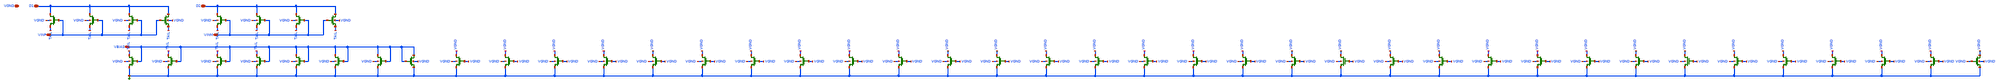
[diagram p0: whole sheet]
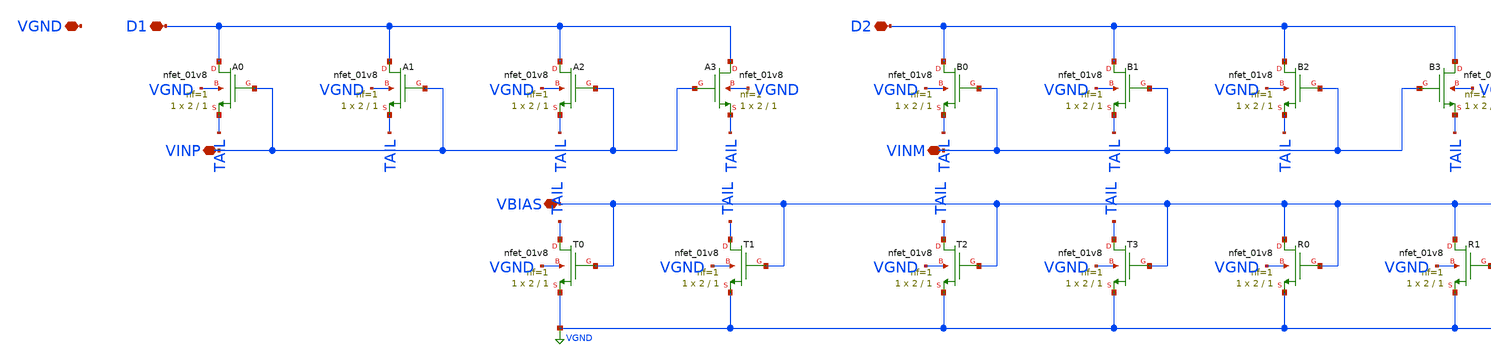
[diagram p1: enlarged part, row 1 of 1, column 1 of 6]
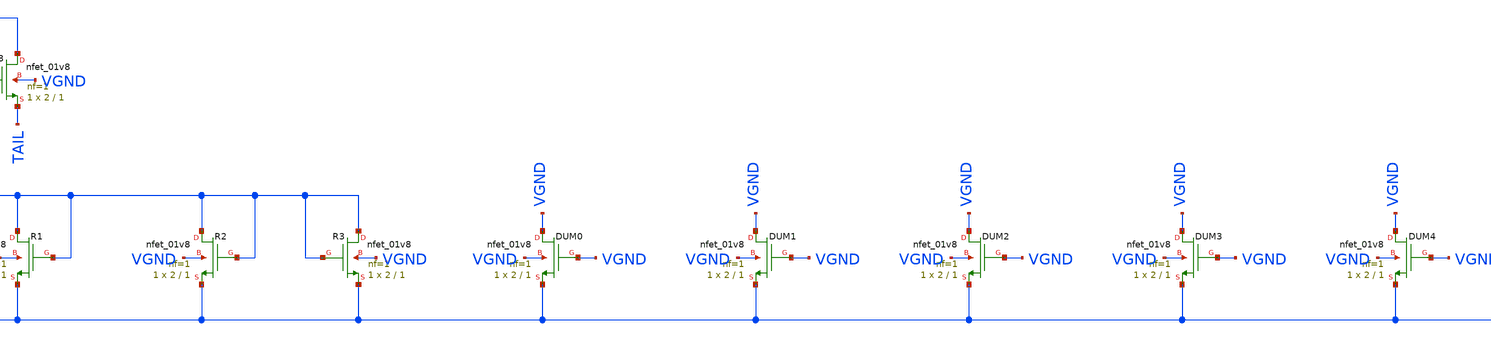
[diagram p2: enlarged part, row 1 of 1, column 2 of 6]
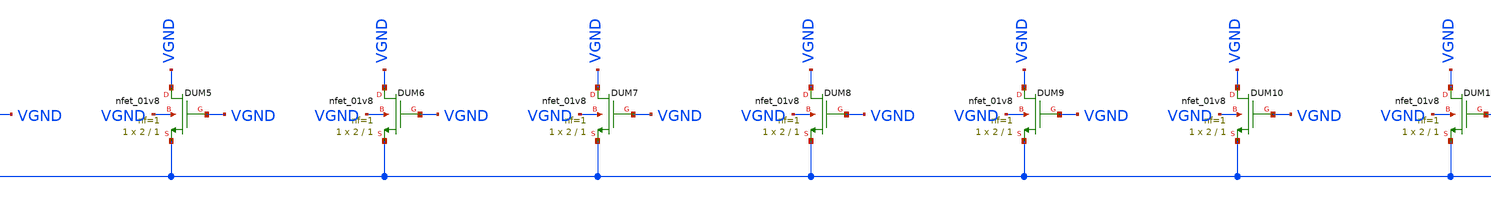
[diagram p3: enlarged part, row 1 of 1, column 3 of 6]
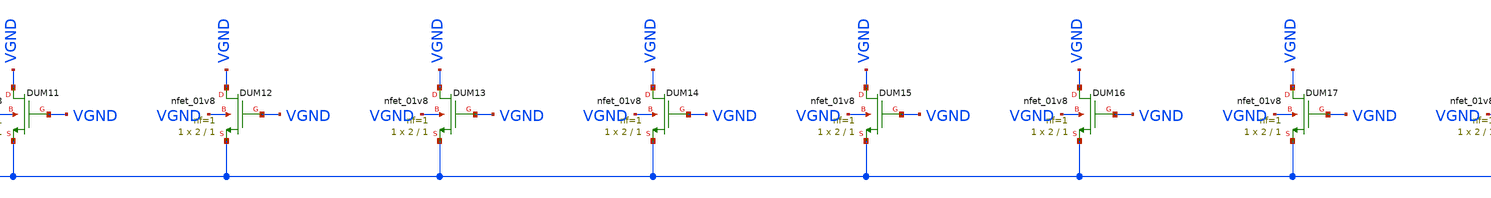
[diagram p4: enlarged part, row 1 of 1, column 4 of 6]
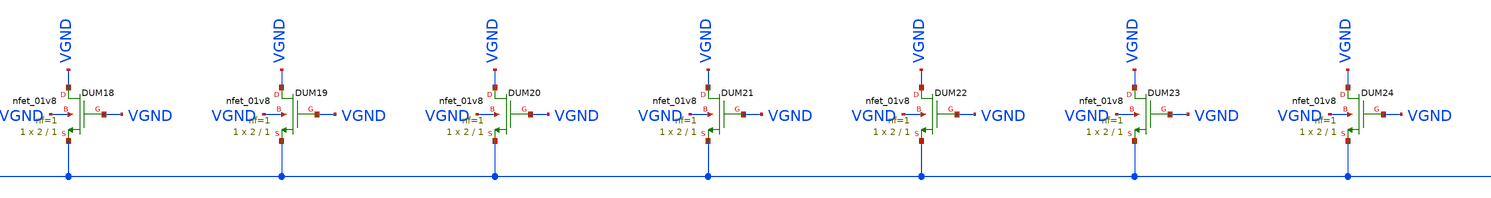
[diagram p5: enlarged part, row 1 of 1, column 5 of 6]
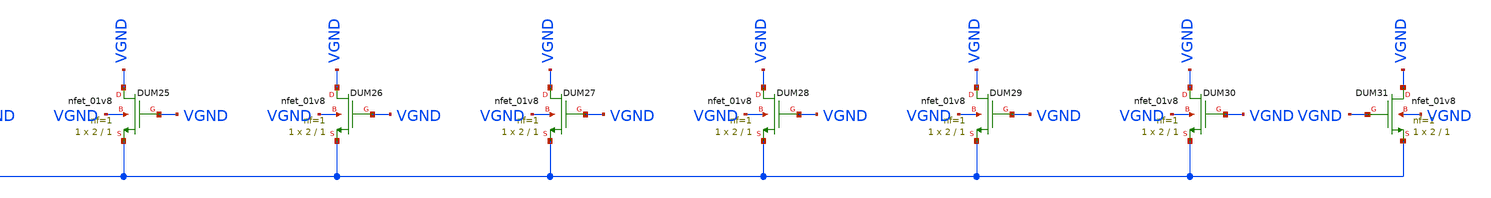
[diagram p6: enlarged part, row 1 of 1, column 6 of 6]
** sch_path: cells/ELAD1_PAIR_GROUPED/schematic/ELAD1_PAIR_GROUPED.sch
**.subckt ELAD1_PAIR_GROUPED VINP VINM D1 D2 VBIAS VGND
*.iopin VINP
*.iopin VINM
*.iopin D1
*.iopin D2
*.iopin VBIAS
*.iopin VGND
XA0 D1 VINP TAIL VGND sky130_fd_pr__nfet_01v8 L=1 W=2 nf=1 ad='int((1 + 1)/2) * 2 / 1 * 0.29' as='int((1 + 2)/2) * 2 / 1 * 0.29'
+ pd='2*int((1 + 1)/2) * (2 / 1 + 0.29)' ps='2*int((1 + 2)/2) * (2 / 1 + 0.29)' nrd='0.29 / 2 ' nrs='0.29 / 2 '
+ sa=0 sb=0 sd=0 mult=1 m=1
XA1 D1 VINP TAIL VGND sky130_fd_pr__nfet_01v8 L=1 W=2 nf=1 ad='int((1 + 1)/2) * 2 / 1 * 0.29' as='int((1 + 2)/2) * 2 / 1 * 0.29'
+ pd='2*int((1 + 1)/2) * (2 / 1 + 0.29)' ps='2*int((1 + 2)/2) * (2 / 1 + 0.29)' nrd='0.29 / 2 ' nrs='0.29 / 2 '
+ sa=0 sb=0 sd=0 mult=1 m=1
XA2 D1 VINP TAIL VGND sky130_fd_pr__nfet_01v8 L=1 W=2 nf=1 ad='int((1 + 1)/2) * 2 / 1 * 0.29' as='int((1 + 2)/2) * 2 / 1 * 0.29'
+ pd='2*int((1 + 1)/2) * (2 / 1 + 0.29)' ps='2*int((1 + 2)/2) * (2 / 1 + 0.29)' nrd='0.29 / 2 ' nrs='0.29 / 2 '
+ sa=0 sb=0 sd=0 mult=1 m=1
XA3 D1 VINP TAIL VGND sky130_fd_pr__nfet_01v8 L=1 W=2 nf=1 ad='int((1 + 1)/2) * 2 / 1 * 0.29' as='int((1 + 2)/2) * 2 / 1 * 0.29'
+ pd='2*int((1 + 1)/2) * (2 / 1 + 0.29)' ps='2*int((1 + 2)/2) * (2 / 1 + 0.29)' nrd='0.29 / 2 ' nrs='0.29 / 2 '
+ sa=0 sb=0 sd=0 mult=1 m=1
XB0 D2 VINM TAIL VGND sky130_fd_pr__nfet_01v8 L=1 W=2 nf=1 ad='int((1 + 1)/2) * 2 / 1 * 0.29' as='int((1 + 2)/2) * 2 / 1 * 0.29'
+ pd='2*int((1 + 1)/2) * (2 / 1 + 0.29)' ps='2*int((1 + 2)/2) * (2 / 1 + 0.29)' nrd='0.29 / 2 ' nrs='0.29 / 2 '
+ sa=0 sb=0 sd=0 mult=1 m=1
XB1 D2 VINM TAIL VGND sky130_fd_pr__nfet_01v8 L=1 W=2 nf=1 ad='int((1 + 1)/2) * 2 / 1 * 0.29' as='int((1 + 2)/2) * 2 / 1 * 0.29'
+ pd='2*int((1 + 1)/2) * (2 / 1 + 0.29)' ps='2*int((1 + 2)/2) * (2 / 1 + 0.29)' nrd='0.29 / 2 ' nrs='0.29 / 2 '
+ sa=0 sb=0 sd=0 mult=1 m=1
XB2 D2 VINM TAIL VGND sky130_fd_pr__nfet_01v8 L=1 W=2 nf=1 ad='int((1 + 1)/2) * 2 / 1 * 0.29' as='int((1 + 2)/2) * 2 / 1 * 0.29'
+ pd='2*int((1 + 1)/2) * (2 / 1 + 0.29)' ps='2*int((1 + 2)/2) * (2 / 1 + 0.29)' nrd='0.29 / 2 ' nrs='0.29 / 2 '
+ sa=0 sb=0 sd=0 mult=1 m=1
XB3 D2 VINM TAIL VGND sky130_fd_pr__nfet_01v8 L=1 W=2 nf=1 ad='int((1 + 1)/2) * 2 / 1 * 0.29' as='int((1 + 2)/2) * 2 / 1 * 0.29'
+ pd='2*int((1 + 1)/2) * (2 / 1 + 0.29)' ps='2*int((1 + 2)/2) * (2 / 1 + 0.29)' nrd='0.29 / 2 ' nrs='0.29 / 2 '
+ sa=0 sb=0 sd=0 mult=1 m=1
XT0 TAIL VBIAS VGND VGND sky130_fd_pr__nfet_01v8 L=1 W=2 nf=1 ad='int((1 + 1)/2) * 2 / 1 * 0.29' as='int((1 + 2)/2) * 2 / 1 * 0.29'
+ pd='2*int((1 + 1)/2) * (2 / 1 + 0.29)' ps='2*int((1 + 2)/2) * (2 / 1 + 0.29)' nrd='0.29 / 2 ' nrs='0.29 / 2 '
+ sa=0 sb=0 sd=0 mult=1 m=1
XT1 TAIL VBIAS VGND VGND sky130_fd_pr__nfet_01v8 L=1 W=2 nf=1 ad='int((1 + 1)/2) * 2 / 1 * 0.29' as='int((1 + 2)/2) * 2 / 1 * 0.29'
+ pd='2*int((1 + 1)/2) * (2 / 1 + 0.29)' ps='2*int((1 + 2)/2) * (2 / 1 + 0.29)' nrd='0.29 / 2 ' nrs='0.29 / 2 '
+ sa=0 sb=0 sd=0 mult=1 m=1
XT2 TAIL VBIAS VGND VGND sky130_fd_pr__nfet_01v8 L=1 W=2 nf=1 ad='int((1 + 1)/2) * 2 / 1 * 0.29' as='int((1 + 2)/2) * 2 / 1 * 0.29'
+ pd='2*int((1 + 1)/2) * (2 / 1 + 0.29)' ps='2*int((1 + 2)/2) * (2 / 1 + 0.29)' nrd='0.29 / 2 ' nrs='0.29 / 2 '
+ sa=0 sb=0 sd=0 mult=1 m=1
XT3 TAIL VBIAS VGND VGND sky130_fd_pr__nfet_01v8 L=1 W=2 nf=1 ad='int((1 + 1)/2) * 2 / 1 * 0.29' as='int((1 + 2)/2) * 2 / 1 * 0.29'
+ pd='2*int((1 + 1)/2) * (2 / 1 + 0.29)' ps='2*int((1 + 2)/2) * (2 / 1 + 0.29)' nrd='0.29 / 2 ' nrs='0.29 / 2 '
+ sa=0 sb=0 sd=0 mult=1 m=1
XR0 VBIAS VBIAS VGND VGND sky130_fd_pr__nfet_01v8 L=1 W=2 nf=1 ad='int((1 + 1)/2) * 2 / 1 * 0.29' as='int((1 + 2)/2) * 2 / 1 * 0.29'
+ pd='2*int((1 + 1)/2) * (2 / 1 + 0.29)' ps='2*int((1 + 2)/2) * (2 / 1 + 0.29)' nrd='0.29 / 2 ' nrs='0.29 / 2 '
+ sa=0 sb=0 sd=0 mult=1 m=1
XR1 VBIAS VBIAS VGND VGND sky130_fd_pr__nfet_01v8 L=1 W=2 nf=1 ad='int((1 + 1)/2) * 2 / 1 * 0.29' as='int((1 + 2)/2) * 2 / 1 * 0.29'
+ pd='2*int((1 + 1)/2) * (2 / 1 + 0.29)' ps='2*int((1 + 2)/2) * (2 / 1 + 0.29)' nrd='0.29 / 2 ' nrs='0.29 / 2 '
+ sa=0 sb=0 sd=0 mult=1 m=1
XR2 VBIAS VBIAS VGND VGND sky130_fd_pr__nfet_01v8 L=1 W=2 nf=1 ad='int((1 + 1)/2) * 2 / 1 * 0.29' as='int((1 + 2)/2) * 2 / 1 * 0.29'
+ pd='2*int((1 + 1)/2) * (2 / 1 + 0.29)' ps='2*int((1 + 2)/2) * (2 / 1 + 0.29)' nrd='0.29 / 2 ' nrs='0.29 / 2 '
+ sa=0 sb=0 sd=0 mult=1 m=1
XR3 VBIAS VBIAS VGND VGND sky130_fd_pr__nfet_01v8 L=1 W=2 nf=1 ad='int((1 + 1)/2) * 2 / 1 * 0.29' as='int((1 + 2)/2) * 2 / 1 * 0.29'
+ pd='2*int((1 + 1)/2) * (2 / 1 + 0.29)' ps='2*int((1 + 2)/2) * (2 / 1 + 0.29)' nrd='0.29 / 2 ' nrs='0.29 / 2 '
+ sa=0 sb=0 sd=0 mult=1 m=1
XDUM0 VGND VGND VGND VGND sky130_fd_pr__nfet_01v8 L=1 W=2 nf=1 ad='int((1 + 1)/2) * 2 / 1 * 0.29' as='int((1 + 2)/2) * 2 / 1 * 0.29'
+ pd='2*int((1 + 1)/2) * (2 / 1 + 0.29)' ps='2*int((1 + 2)/2) * (2 / 1 + 0.29)' nrd='0.29 / 2 ' nrs='0.29 / 2 '
+ sa=0 sb=0 sd=0 mult=1 m=1
XDUM1 VGND VGND VGND VGND sky130_fd_pr__nfet_01v8 L=1 W=2 nf=1 ad='int((1 + 1)/2) * 2 / 1 * 0.29' as='int((1 + 2)/2) * 2 / 1 * 0.29'
+ pd='2*int((1 + 1)/2) * (2 / 1 + 0.29)' ps='2*int((1 + 2)/2) * (2 / 1 + 0.29)' nrd='0.29 / 2 ' nrs='0.29 / 2 '
+ sa=0 sb=0 sd=0 mult=1 m=1
XDUM2 VGND VGND VGND VGND sky130_fd_pr__nfet_01v8 L=1 W=2 nf=1 ad='int((1 + 1)/2) * 2 / 1 * 0.29' as='int((1 + 2)/2) * 2 / 1 * 0.29'
+ pd='2*int((1 + 1)/2) * (2 / 1 + 0.29)' ps='2*int((1 + 2)/2) * (2 / 1 + 0.29)' nrd='0.29 / 2 ' nrs='0.29 / 2 '
+ sa=0 sb=0 sd=0 mult=1 m=1
XDUM3 VGND VGND VGND VGND sky130_fd_pr__nfet_01v8 L=1 W=2 nf=1 ad='int((1 + 1)/2) * 2 / 1 * 0.29' as='int((1 + 2)/2) * 2 / 1 * 0.29'
+ pd='2*int((1 + 1)/2) * (2 / 1 + 0.29)' ps='2*int((1 + 2)/2) * (2 / 1 + 0.29)' nrd='0.29 / 2 ' nrs='0.29 / 2 '
+ sa=0 sb=0 sd=0 mult=1 m=1
XDUM4 VGND VGND VGND VGND sky130_fd_pr__nfet_01v8 L=1 W=2 nf=1 ad='int((1 + 1)/2) * 2 / 1 * 0.29' as='int((1 + 2)/2) * 2 / 1 * 0.29'
+ pd='2*int((1 + 1)/2) * (2 / 1 + 0.29)' ps='2*int((1 + 2)/2) * (2 / 1 + 0.29)' nrd='0.29 / 2 ' nrs='0.29 / 2 '
+ sa=0 sb=0 sd=0 mult=1 m=1
XDUM5 VGND VGND VGND VGND sky130_fd_pr__nfet_01v8 L=1 W=2 nf=1 ad='int((1 + 1)/2) * 2 / 1 * 0.29' as='int((1 + 2)/2) * 2 / 1 * 0.29'
+ pd='2*int((1 + 1)/2) * (2 / 1 + 0.29)' ps='2*int((1 + 2)/2) * (2 / 1 + 0.29)' nrd='0.29 / 2 ' nrs='0.29 / 2 '
+ sa=0 sb=0 sd=0 mult=1 m=1
XDUM6 VGND VGND VGND VGND sky130_fd_pr__nfet_01v8 L=1 W=2 nf=1 ad='int((1 + 1)/2) * 2 / 1 * 0.29' as='int((1 + 2)/2) * 2 / 1 * 0.29'
+ pd='2*int((1 + 1)/2) * (2 / 1 + 0.29)' ps='2*int((1 + 2)/2) * (2 / 1 + 0.29)' nrd='0.29 / 2 ' nrs='0.29 / 2 '
+ sa=0 sb=0 sd=0 mult=1 m=1
XDUM7 VGND VGND VGND VGND sky130_fd_pr__nfet_01v8 L=1 W=2 nf=1 ad='int((1 + 1)/2) * 2 / 1 * 0.29' as='int((1 + 2)/2) * 2 / 1 * 0.29'
+ pd='2*int((1 + 1)/2) * (2 / 1 + 0.29)' ps='2*int((1 + 2)/2) * (2 / 1 + 0.29)' nrd='0.29 / 2 ' nrs='0.29 / 2 '
+ sa=0 sb=0 sd=0 mult=1 m=1
XDUM8 VGND VGND VGND VGND sky130_fd_pr__nfet_01v8 L=1 W=2 nf=1 ad='int((1 + 1)/2) * 2 / 1 * 0.29' as='int((1 + 2)/2) * 2 / 1 * 0.29'
+ pd='2*int((1 + 1)/2) * (2 / 1 + 0.29)' ps='2*int((1 + 2)/2) * (2 / 1 + 0.29)' nrd='0.29 / 2 ' nrs='0.29 / 2 '
+ sa=0 sb=0 sd=0 mult=1 m=1
XDUM9 VGND VGND VGND VGND sky130_fd_pr__nfet_01v8 L=1 W=2 nf=1 ad='int((1 + 1)/2) * 2 / 1 * 0.29' as='int((1 + 2)/2) * 2 / 1 * 0.29'
+ pd='2*int((1 + 1)/2) * (2 / 1 + 0.29)' ps='2*int((1 + 2)/2) * (2 / 1 + 0.29)' nrd='0.29 / 2 ' nrs='0.29 / 2 '
+ sa=0 sb=0 sd=0 mult=1 m=1
XDUM10 VGND VGND VGND VGND sky130_fd_pr__nfet_01v8 L=1 W=2 nf=1 ad='int((1 + 1)/2) * 2 / 1 * 0.29' as='int((1 + 2)/2) * 2 / 1 * 0.29'
+ pd='2*int((1 + 1)/2) * (2 / 1 + 0.29)' ps='2*int((1 + 2)/2) * (2 / 1 + 0.29)' nrd='0.29 / 2 ' nrs='0.29 / 2 '
+ sa=0 sb=0 sd=0 mult=1 m=1
XDUM11 VGND VGND VGND VGND sky130_fd_pr__nfet_01v8 L=1 W=2 nf=1 ad='int((1 + 1)/2) * 2 / 1 * 0.29' as='int((1 + 2)/2) * 2 / 1 * 0.29'
+ pd='2*int((1 + 1)/2) * (2 / 1 + 0.29)' ps='2*int((1 + 2)/2) * (2 / 1 + 0.29)' nrd='0.29 / 2 ' nrs='0.29 / 2 '
+ sa=0 sb=0 sd=0 mult=1 m=1
XDUM12 VGND VGND VGND VGND sky130_fd_pr__nfet_01v8 L=1 W=2 nf=1 ad='int((1 + 1)/2) * 2 / 1 * 0.29' as='int((1 + 2)/2) * 2 / 1 * 0.29'
+ pd='2*int((1 + 1)/2) * (2 / 1 + 0.29)' ps='2*int((1 + 2)/2) * (2 / 1 + 0.29)' nrd='0.29 / 2 ' nrs='0.29 / 2 '
+ sa=0 sb=0 sd=0 mult=1 m=1
XDUM13 VGND VGND VGND VGND sky130_fd_pr__nfet_01v8 L=1 W=2 nf=1 ad='int((1 + 1)/2) * 2 / 1 * 0.29' as='int((1 + 2)/2) * 2 / 1 * 0.29'
+ pd='2*int((1 + 1)/2) * (2 / 1 + 0.29)' ps='2*int((1 + 2)/2) * (2 / 1 + 0.29)' nrd='0.29 / 2 ' nrs='0.29 / 2 '
+ sa=0 sb=0 sd=0 mult=1 m=1
XDUM14 VGND VGND VGND VGND sky130_fd_pr__nfet_01v8 L=1 W=2 nf=1 ad='int((1 + 1)/2) * 2 / 1 * 0.29' as='int((1 + 2)/2) * 2 / 1 * 0.29'
+ pd='2*int((1 + 1)/2) * (2 / 1 + 0.29)' ps='2*int((1 + 2)/2) * (2 / 1 + 0.29)' nrd='0.29 / 2 ' nrs='0.29 / 2 '
+ sa=0 sb=0 sd=0 mult=1 m=1
XDUM15 VGND VGND VGND VGND sky130_fd_pr__nfet_01v8 L=1 W=2 nf=1 ad='int((1 + 1)/2) * 2 / 1 * 0.29' as='int((1 + 2)/2) * 2 / 1 * 0.29'
+ pd='2*int((1 + 1)/2) * (2 / 1 + 0.29)' ps='2*int((1 + 2)/2) * (2 / 1 + 0.29)' nrd='0.29 / 2 ' nrs='0.29 / 2 '
+ sa=0 sb=0 sd=0 mult=1 m=1
XDUM16 VGND VGND VGND VGND sky130_fd_pr__nfet_01v8 L=1 W=2 nf=1 ad='int((1 + 1)/2) * 2 / 1 * 0.29' as='int((1 + 2)/2) * 2 / 1 * 0.29'
+ pd='2*int((1 + 1)/2) * (2 / 1 + 0.29)' ps='2*int((1 + 2)/2) * (2 / 1 + 0.29)' nrd='0.29 / 2 ' nrs='0.29 / 2 '
+ sa=0 sb=0 sd=0 mult=1 m=1
XDUM17 VGND VGND VGND VGND sky130_fd_pr__nfet_01v8 L=1 W=2 nf=1 ad='int((1 + 1)/2) * 2 / 1 * 0.29' as='int((1 + 2)/2) * 2 / 1 * 0.29'
+ pd='2*int((1 + 1)/2) * (2 / 1 + 0.29)' ps='2*int((1 + 2)/2) * (2 / 1 + 0.29)' nrd='0.29 / 2 ' nrs='0.29 / 2 '
+ sa=0 sb=0 sd=0 mult=1 m=1
XDUM18 VGND VGND VGND VGND sky130_fd_pr__nfet_01v8 L=1 W=2 nf=1 ad='int((1 + 1)/2) * 2 / 1 * 0.29' as='int((1 + 2)/2) * 2 / 1 * 0.29'
+ pd='2*int((1 + 1)/2) * (2 / 1 + 0.29)' ps='2*int((1 + 2)/2) * (2 / 1 + 0.29)' nrd='0.29 / 2 ' nrs='0.29 / 2 '
+ sa=0 sb=0 sd=0 mult=1 m=1
XDUM19 VGND VGND VGND VGND sky130_fd_pr__nfet_01v8 L=1 W=2 nf=1 ad='int((1 + 1)/2) * 2 / 1 * 0.29' as='int((1 + 2)/2) * 2 / 1 * 0.29'
+ pd='2*int((1 + 1)/2) * (2 / 1 + 0.29)' ps='2*int((1 + 2)/2) * (2 / 1 + 0.29)' nrd='0.29 / 2 ' nrs='0.29 / 2 '
+ sa=0 sb=0 sd=0 mult=1 m=1
XDUM20 VGND VGND VGND VGND sky130_fd_pr__nfet_01v8 L=1 W=2 nf=1 ad='int((1 + 1)/2) * 2 / 1 * 0.29' as='int((1 + 2)/2) * 2 / 1 * 0.29'
+ pd='2*int((1 + 1)/2) * (2 / 1 + 0.29)' ps='2*int((1 + 2)/2) * (2 / 1 + 0.29)' nrd='0.29 / 2 ' nrs='0.29 / 2 '
+ sa=0 sb=0 sd=0 mult=1 m=1
XDUM21 VGND VGND VGND VGND sky130_fd_pr__nfet_01v8 L=1 W=2 nf=1 ad='int((1 + 1)/2) * 2 / 1 * 0.29' as='int((1 + 2)/2) * 2 / 1 * 0.29'
+ pd='2*int((1 + 1)/2) * (2 / 1 + 0.29)' ps='2*int((1 + 2)/2) * (2 / 1 + 0.29)' nrd='0.29 / 2 ' nrs='0.29 / 2 '
+ sa=0 sb=0 sd=0 mult=1 m=1
XDUM22 VGND VGND VGND VGND sky130_fd_pr__nfet_01v8 L=1 W=2 nf=1 ad='int((1 + 1)/2) * 2 / 1 * 0.29' as='int((1 + 2)/2) * 2 / 1 * 0.29'
+ pd='2*int((1 + 1)/2) * (2 / 1 + 0.29)' ps='2*int((1 + 2)/2) * (2 / 1 + 0.29)' nrd='0.29 / 2 ' nrs='0.29 / 2 '
+ sa=0 sb=0 sd=0 mult=1 m=1
XDUM23 VGND VGND VGND VGND sky130_fd_pr__nfet_01v8 L=1 W=2 nf=1 ad='int((1 + 1)/2) * 2 / 1 * 0.29' as='int((1 + 2)/2) * 2 / 1 * 0.29'
+ pd='2*int((1 + 1)/2) * (2 / 1 + 0.29)' ps='2*int((1 + 2)/2) * (2 / 1 + 0.29)' nrd='0.29 / 2 ' nrs='0.29 / 2 '
+ sa=0 sb=0 sd=0 mult=1 m=1
XDUM24 VGND VGND VGND VGND sky130_fd_pr__nfet_01v8 L=1 W=2 nf=1 ad='int((1 + 1)/2) * 2 / 1 * 0.29' as='int((1 + 2)/2) * 2 / 1 * 0.29'
+ pd='2*int((1 + 1)/2) * (2 / 1 + 0.29)' ps='2*int((1 + 2)/2) * (2 / 1 + 0.29)' nrd='0.29 / 2 ' nrs='0.29 / 2 '
+ sa=0 sb=0 sd=0 mult=1 m=1
XDUM25 VGND VGND VGND VGND sky130_fd_pr__nfet_01v8 L=1 W=2 nf=1 ad='int((1 + 1)/2) * 2 / 1 * 0.29' as='int((1 + 2)/2) * 2 / 1 * 0.29'
+ pd='2*int((1 + 1)/2) * (2 / 1 + 0.29)' ps='2*int((1 + 2)/2) * (2 / 1 + 0.29)' nrd='0.29 / 2 ' nrs='0.29 / 2 '
+ sa=0 sb=0 sd=0 mult=1 m=1
XDUM26 VGND VGND VGND VGND sky130_fd_pr__nfet_01v8 L=1 W=2 nf=1 ad='int((1 + 1)/2) * 2 / 1 * 0.29' as='int((1 + 2)/2) * 2 / 1 * 0.29'
+ pd='2*int((1 + 1)/2) * (2 / 1 + 0.29)' ps='2*int((1 + 2)/2) * (2 / 1 + 0.29)' nrd='0.29 / 2 ' nrs='0.29 / 2 '
+ sa=0 sb=0 sd=0 mult=1 m=1
XDUM27 VGND VGND VGND VGND sky130_fd_pr__nfet_01v8 L=1 W=2 nf=1 ad='int((1 + 1)/2) * 2 / 1 * 0.29' as='int((1 + 2)/2) * 2 / 1 * 0.29'
+ pd='2*int((1 + 1)/2) * (2 / 1 + 0.29)' ps='2*int((1 + 2)/2) * (2 / 1 + 0.29)' nrd='0.29 / 2 ' nrs='0.29 / 2 '
+ sa=0 sb=0 sd=0 mult=1 m=1
XDUM28 VGND VGND VGND VGND sky130_fd_pr__nfet_01v8 L=1 W=2 nf=1 ad='int((1 + 1)/2) * 2 / 1 * 0.29' as='int((1 + 2)/2) * 2 / 1 * 0.29'
+ pd='2*int((1 + 1)/2) * (2 / 1 + 0.29)' ps='2*int((1 + 2)/2) * (2 / 1 + 0.29)' nrd='0.29 / 2 ' nrs='0.29 / 2 '
+ sa=0 sb=0 sd=0 mult=1 m=1
XDUM29 VGND VGND VGND VGND sky130_fd_pr__nfet_01v8 L=1 W=2 nf=1 ad='int((1 + 1)/2) * 2 / 1 * 0.29' as='int((1 + 2)/2) * 2 / 1 * 0.29'
+ pd='2*int((1 + 1)/2) * (2 / 1 + 0.29)' ps='2*int((1 + 2)/2) * (2 / 1 + 0.29)' nrd='0.29 / 2 ' nrs='0.29 / 2 '
+ sa=0 sb=0 sd=0 mult=1 m=1
XDUM30 VGND VGND VGND VGND sky130_fd_pr__nfet_01v8 L=1 W=2 nf=1 ad='int((1 + 1)/2) * 2 / 1 * 0.29' as='int((1 + 2)/2) * 2 / 1 * 0.29'
+ pd='2*int((1 + 1)/2) * (2 / 1 + 0.29)' ps='2*int((1 + 2)/2) * (2 / 1 + 0.29)' nrd='0.29 / 2 ' nrs='0.29 / 2 '
+ sa=0 sb=0 sd=0 mult=1 m=1
XDUM31 VGND VGND VGND VGND sky130_fd_pr__nfet_01v8 L=1 W=2 nf=1 ad='int((1 + 1)/2) * 2 / 1 * 0.29' as='int((1 + 2)/2) * 2 / 1 * 0.29'
+ pd='2*int((1 + 1)/2) * (2 / 1 + 0.29)' ps='2*int((1 + 2)/2) * (2 / 1 + 0.29)' nrd='0.29 / 2 ' nrs='0.29 / 2 '
+ sa=0 sb=0 sd=0 mult=1 m=1
**.ends
.GLOBAL VGND
.end
